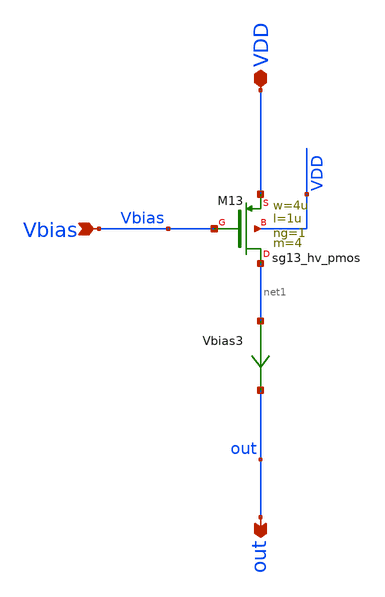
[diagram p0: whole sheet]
** sch_path: xschem/V2I/Idc.sch
**.subckt Idc VDD Vbias out
*.iopin VDD
*.ipin Vbias
*.opin out
Vbias3 net1 out 0
.save i(vbias3)
XM13 net1 Vbias VDD VDD sg13_hv_pmos w=4u l=1u ng=1 m=4 mm_ok=1
**.ends
.end
